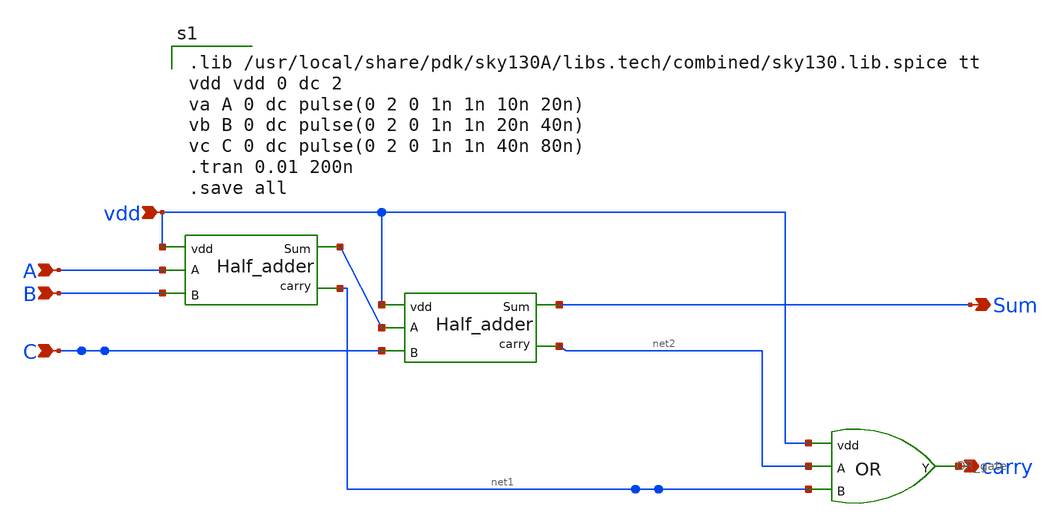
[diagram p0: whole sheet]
** sch_path: Circuit Files/circuits/circuits/Full_adder.sch
**.subckt Full_adder A B C vdd carry Sum
*.ipin A
*.ipin B
*.ipin C
*.ipin vdd
*.opin carry
*.opin Sum
x2 A vdd net3 B net1 half_adder
x3 net3 vdd Sum C net2 half_adder
x1 vdd net2 net1 carry OR_gate
**** begin user architecture code

.lib /usr/local/share/pdk/sky130A/libs.tech/combined/sky130.lib.spice tt
vdd vdd 0 dc 2
va A 0 dc pulse(0 2 0 1n 1n 10n 20n)
vb B 0 dc pulse(0 2 0 1n 1n 20n 40n)
vc C 0 dc pulse(0 2 0 1n 1n 40n 80n)
.tran 0.01 200n
.save all

**** end user architecture code
**.ends

* expanding   symbol:  daVLSI_World/circuits/half_adder.sym # of pins=5
** sym_path: Circuit Files/circuits/circuits/half_adder.sym
** sch_path: Circuit Files/circuits/circuits/half_adder.sch
.subckt half_adder A vdd Sum B carry
*.ipin A
*.ipin vdd
*.ipin B
*.opin Sum
*.opin carry
**** begin user architecture code

.lib /usr/local/share/pdk/sky130A/libs.tech/combined/sky130.lib.spice tt
vdd vdd 0 dc 2
va A 0 dc pulse(0 2 0 1n 1n 10n 20n)
vb B 0 dc pulse(0 2 0 1n 1n 20n 40n)
.tran 0.1 100n
.save all

**** end user architecture code
x2 A vdd carry B AND_gate
x1 A vdd Sum B XOR_gate
.ends


* expanding   symbol:  daVLSI_World/gates/OR_gate.sym # of pins=4
** sym_path: Circuit Files/Logic gate design using MOSFETS/gates/OR_gate.sym
** sch_path: Circuit Files/Logic gate design using MOSFETS/gates/OR_gate.sch
.subckt OR_gate vdd A B Y
*.ipin A
*.ipin B
*.ipin vdd
*.opin Y
XM1 net1 B net2 vdd sky130_fd_pr__pfet_01v8 L=0.15 W=2 nf=1 ad='int((nf+1)/2) * W/nf * 0.29' as='int((nf+2)/2) * W/nf * 0.29'
+ pd='2*int((nf+1)/2) * (W/nf + 0.29)' ps='2*int((nf+2)/2) * (W/nf + 0.29)' nrd='0.29 / W' nrs='0.29 / W'
+ sa=0 sb=0 sd=0 mult=1 m=1
XM2 net2 A vdd vdd sky130_fd_pr__pfet_01v8 L=0.15 W=2 nf=1 ad='int((nf+1)/2) * W/nf * 0.29' as='int((nf+2)/2) * W/nf * 0.29'
+ pd='2*int((nf+1)/2) * (W/nf + 0.29)' ps='2*int((nf+2)/2) * (W/nf + 0.29)' nrd='0.29 / W' nrs='0.29 / W'
+ sa=0 sb=0 sd=0 mult=1 m=1
XM3 net1 B GND GND sky130_fd_pr__nfet_01v8 L=0.15 W=1 nf=1 ad='int((nf+1)/2) * W/nf * 0.29' as='int((nf+2)/2) * W/nf * 0.29'
+ pd='2*int((nf+1)/2) * (W/nf + 0.29)' ps='2*int((nf+2)/2) * (W/nf + 0.29)' nrd='0.29 / W' nrs='0.29 / W'
+ sa=0 sb=0 sd=0 mult=1 m=1
XM4 net1 A GND GND sky130_fd_pr__nfet_01v8 L=0.15 W=1 nf=1 ad='int((nf+1)/2) * W/nf * 0.29' as='int((nf+2)/2) * W/nf * 0.29'
+ pd='2*int((nf+1)/2) * (W/nf + 0.29)' ps='2*int((nf+2)/2) * (W/nf + 0.29)' nrd='0.29 / W' nrs='0.29 / W'
+ sa=0 sb=0 sd=0 mult=1 m=1
XM9 Y net1 vdd vdd sky130_fd_pr__pfet_01v8 L=0.15 W=2 nf=1 ad='int((nf+1)/2) * W/nf * 0.29' as='int((nf+2)/2) * W/nf * 0.29'
+ pd='2*int((nf+1)/2) * (W/nf + 0.29)' ps='2*int((nf+2)/2) * (W/nf + 0.29)' nrd='0.29 / W' nrs='0.29 / W'
+ sa=0 sb=0 sd=0 mult=1 m=1
XM10 Y net1 GND GND sky130_fd_pr__nfet_01v8 L=0.15 W=1 nf=1 ad='int((nf+1)/2) * W/nf * 0.29' as='int((nf+2)/2) * W/nf * 0.29'
+ pd='2*int((nf+1)/2) * (W/nf + 0.29)' ps='2*int((nf+2)/2) * (W/nf + 0.29)' nrd='0.29 / W' nrs='0.29 / W'
+ sa=0 sb=0 sd=0 mult=1 m=1
.ends


* expanding   symbol:  daVLSI_World/gates/AND_gate.sym # of pins=4
** sym_path: Circuit Files/Logic gate design using MOSFETS/gates/AND_gate.sym
** sch_path: Circuit Files/Logic gate design using MOSFETS/gates/AND_gate.sch
.subckt AND_gate vdd A Y B
*.opin Y
*.ipin A
*.ipin B
*.ipin vdd
x1 vdd net1 A B GND NAND_gate
x2 vdd net1 Y inverter_vtc
.ends


* expanding   symbol:  daVLSI_World/gates/XOR_gate.sym # of pins=4
** sym_path: Circuit Files/Logic gate design using MOSFETS/gates/XOR_gate.sym
** sch_path: Circuit Files/Logic gate design using MOSFETS/gates/XOR_gate.sch
.subckt XOR_gate A vdd Y B
*.opin Y
*.ipin A
*.ipin B
*.ipin vdd
XM1 Y A net2 GND sky130_fd_pr__nfet_01v8 L=0.15 W=1 nf=1 ad='int((nf+1)/2) * W/nf * 0.29' as='int((nf+2)/2) * W/nf * 0.29'
+ pd='2*int((nf+1)/2) * (W/nf + 0.29)' ps='2*int((nf+2)/2) * (W/nf + 0.29)' nrd='0.29 / W' nrs='0.29 / W'
+ sa=0 sb=0 sd=0 mult=1 m=1
XM2 Y Ai net3 GND sky130_fd_pr__nfet_01v8 L=0.15 W=1 nf=1 ad='int((nf+1)/2) * W/nf * 0.29' as='int((nf+2)/2) * W/nf * 0.29'
+ pd='2*int((nf+1)/2) * (W/nf + 0.29)' ps='2*int((nf+2)/2) * (W/nf + 0.29)' nrd='0.29 / W' nrs='0.29 / W'
+ sa=0 sb=0 sd=0 mult=1 m=1
XM3 net2 B GND GND sky130_fd_pr__nfet_01v8 L=0.15 W=1 nf=1 ad='int((nf+1)/2) * W/nf * 0.29' as='int((nf+2)/2) * W/nf * 0.29'
+ pd='2*int((nf+1)/2) * (W/nf + 0.29)' ps='2*int((nf+2)/2) * (W/nf + 0.29)' nrd='0.29 / W' nrs='0.29 / W'
+ sa=0 sb=0 sd=0 mult=1 m=1
XM4 net3 Bi GND GND sky130_fd_pr__nfet_01v8 L=0.15 W=1 nf=1 ad='int((nf+1)/2) * W/nf * 0.29' as='int((nf+2)/2) * W/nf * 0.29'
+ pd='2*int((nf+1)/2) * (W/nf + 0.29)' ps='2*int((nf+2)/2) * (W/nf + 0.29)' nrd='0.29 / W' nrs='0.29 / W'
+ sa=0 sb=0 sd=0 mult=1 m=1
XM5 Y Ai net1 vdd sky130_fd_pr__pfet_01v8 L=0.15 W=2 nf=1 ad='int((nf+1)/2) * W/nf * 0.29' as='int((nf+2)/2) * W/nf * 0.29'
+ pd='2*int((nf+1)/2) * (W/nf + 0.29)' ps='2*int((nf+2)/2) * (W/nf + 0.29)' nrd='0.29 / W' nrs='0.29 / W'
+ sa=0 sb=0 sd=0 mult=1 m=1
XM6 Y Bi net1 vdd sky130_fd_pr__pfet_01v8 L=0.15 W=2 nf=1 ad='int((nf+1)/2) * W/nf * 0.29' as='int((nf+2)/2) * W/nf * 0.29'
+ pd='2*int((nf+1)/2) * (W/nf + 0.29)' ps='2*int((nf+2)/2) * (W/nf + 0.29)' nrd='0.29 / W' nrs='0.29 / W'
+ sa=0 sb=0 sd=0 mult=1 m=1
XM7 net1 A vdd vdd sky130_fd_pr__pfet_01v8 L=0.15 W=2 nf=1 ad='int((nf+1)/2) * W/nf * 0.29' as='int((nf+2)/2) * W/nf * 0.29'
+ pd='2*int((nf+1)/2) * (W/nf + 0.29)' ps='2*int((nf+2)/2) * (W/nf + 0.29)' nrd='0.29 / W' nrs='0.29 / W'
+ sa=0 sb=0 sd=0 mult=1 m=1
XM8 net1 B vdd vdd sky130_fd_pr__pfet_01v8 L=0.15 W=2 nf=1 ad='int((nf+1)/2) * W/nf * 0.29' as='int((nf+2)/2) * W/nf * 0.29'
+ pd='2*int((nf+1)/2) * (W/nf + 0.29)' ps='2*int((nf+2)/2) * (W/nf + 0.29)' nrd='0.29 / W' nrs='0.29 / W'
+ sa=0 sb=0 sd=0 mult=1 m=1
XM9 Ai A vdd vdd sky130_fd_pr__pfet_01v8 L=0.15 W=2 nf=1 ad='int((nf+1)/2) * W/nf * 0.29' as='int((nf+2)/2) * W/nf * 0.29'
+ pd='2*int((nf+1)/2) * (W/nf + 0.29)' ps='2*int((nf+2)/2) * (W/nf + 0.29)' nrd='0.29 / W' nrs='0.29 / W'
+ sa=0 sb=0 sd=0 mult=1 m=1
XM10 Ai A GND GND sky130_fd_pr__nfet_01v8 L=0.15 W=1 nf=1 ad='int((nf+1)/2) * W/nf * 0.29' as='int((nf+2)/2) * W/nf * 0.29'
+ pd='2*int((nf+1)/2) * (W/nf + 0.29)' ps='2*int((nf+2)/2) * (W/nf + 0.29)' nrd='0.29 / W' nrs='0.29 / W'
+ sa=0 sb=0 sd=0 mult=1 m=1
XM11 Bi B vdd vdd sky130_fd_pr__pfet_01v8 L=0.15 W=2 nf=1 ad='int((nf+1)/2) * W/nf * 0.29' as='int((nf+2)/2) * W/nf * 0.29'
+ pd='2*int((nf+1)/2) * (W/nf + 0.29)' ps='2*int((nf+2)/2) * (W/nf + 0.29)' nrd='0.29 / W' nrs='0.29 / W'
+ sa=0 sb=0 sd=0 mult=1 m=1
XM12 Bi B GND GND sky130_fd_pr__nfet_01v8 L=0.15 W=1 nf=1 ad='int((nf+1)/2) * W/nf * 0.29' as='int((nf+2)/2) * W/nf * 0.29'
+ pd='2*int((nf+1)/2) * (W/nf + 0.29)' ps='2*int((nf+2)/2) * (W/nf + 0.29)' nrd='0.29 / W' nrs='0.29 / W'
+ sa=0 sb=0 sd=0 mult=1 m=1
.ends


* expanding   symbol:  daVLSI_World/gates/NAND_gate.sym # of pins=5
** sym_path: Circuit Files/Logic gate design using MOSFETS/gates/NAND_gate.sym
** sch_path: Circuit Files/Logic gate design using MOSFETS/gates/NAND_gate.sch
.subckt NAND_gate vdd Y A B gnd
*.ipin A
*.ipin B
*.opin Y
*.ipin vdd
*.ipin gnd
XM1 Y A net1 gnd sky130_fd_pr__nfet_01v8 L=0.15 W=1 nf=1 ad='int((nf+1)/2) * W/nf * 0.29' as='int((nf+2)/2) * W/nf * 0.29'
+ pd='2*int((nf+1)/2) * (W/nf + 0.29)' ps='2*int((nf+2)/2) * (W/nf + 0.29)' nrd='0.29 / W' nrs='0.29 / W'
+ sa=0 sb=0 sd=0 mult=1 m=1
XM2 net1 B gnd gnd sky130_fd_pr__nfet_01v8 L=0.15 W=1 nf=1 ad='int((nf+1)/2) * W/nf * 0.29' as='int((nf+2)/2) * W/nf * 0.29'
+ pd='2*int((nf+1)/2) * (W/nf + 0.29)' ps='2*int((nf+2)/2) * (W/nf + 0.29)' nrd='0.29 / W' nrs='0.29 / W'
+ sa=0 sb=0 sd=0 mult=1 m=1
XM3 Y A vdd vdd sky130_fd_pr__pfet_01v8 L=0.15 W=2 nf=1 ad='int((nf+1)/2) * W/nf * 0.29' as='int((nf+2)/2) * W/nf * 0.29'
+ pd='2*int((nf+1)/2) * (W/nf + 0.29)' ps='2*int((nf+2)/2) * (W/nf + 0.29)' nrd='0.29 / W' nrs='0.29 / W'
+ sa=0 sb=0 sd=0 mult=1 m=1
XM4 Y B vdd vdd sky130_fd_pr__pfet_01v8 L=0.15 W=2 nf=1 ad='int((nf+1)/2) * W/nf * 0.29' as='int((nf+2)/2) * W/nf * 0.29'
+ pd='2*int((nf+1)/2) * (W/nf + 0.29)' ps='2*int((nf+2)/2) * (W/nf + 0.29)' nrd='0.29 / W' nrs='0.29 / W'
+ sa=0 sb=0 sd=0 mult=1 m=1
.ends


* expanding   symbol:  daVLSI_World/gates/inverter_vtc.sym # of pins=3
** sym_path: Circuit Files/Logic gate design using MOSFETS/gates/inverter_vtc.sym
** sch_path: Circuit Files/Logic gate design using MOSFETS/gates/inverter_vtc.sch
.subckt inverter_vtc vdd vin vout
*.ipin vin
*.opin vout
*.ipin vdd
XM1 vout vin GND GND sky130_fd_pr__nfet_01v8 L=0.15 W=1 nf=1 ad='int((nf+1)/2) * W/nf * 0.29' as='int((nf+2)/2) * W/nf * 0.29'
+ pd='2*int((nf+1)/2) * (W/nf + 0.29)' ps='2*int((nf+2)/2) * (W/nf + 0.29)' nrd='0.29 / W' nrs='0.29 / W'
+ sa=0 sb=0 sd=0 mult=1 m=1
XM2 vout vin vdd vdd sky130_fd_pr__pfet_01v8 L=0.15 W=2 nf=1 ad='int((nf+1)/2) * W/nf * 0.29' as='int((nf+2)/2) * W/nf * 0.29'
+ pd='2*int((nf+1)/2) * (W/nf + 0.29)' ps='2*int((nf+2)/2) * (W/nf + 0.29)' nrd='0.29 / W' nrs='0.29 / W'
+ sa=0 sb=0 sd=0 mult=1 m=1
.ends

.GLOBAL GND
.end
